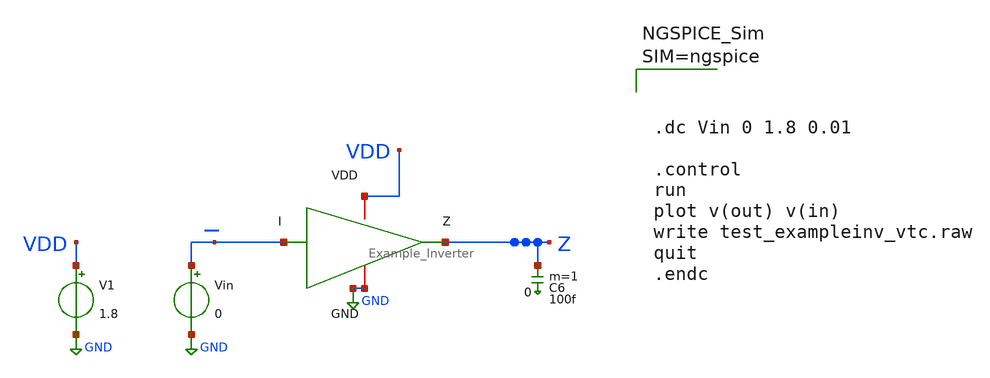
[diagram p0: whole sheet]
** sch_path: sky130_cells/Practice/Example_Inverter/Sims/Example_Inverter_TB_VTC.sch
**.subckt Example_Inverter_TB_VTC
V1 VDD GND 1.8
Vin I GND 0
C6 Z 0 100f m=1
x1 VDD I Z GND Example_Inverter
**** begin user architecture code
 .lib /usr/local/share/pdk/sky130A/libs.tech/ngspice/sky130.lib.spice tt




.dc Vin 0 1.8 0.01

.control
run
plot v(out) v(in)
write test_exampleinv_vtc.raw
quit
.endc



**** end user architecture code
**.ends

* expanding   symbol:  sky130_cells/Practice/Example_Inverter/Example_Inverter.sym # of pins=4
** sym_path: sky130_cells/Practice/Example_Inverter/Example_Inverter.sym
** sch_path: sky130_cells/Practice/Example_Inverter/Example_Inverter.sch
.subckt Example_Inverter VDD I Z GND
*.ipin I
*.opin Z
*.iopin VDD
*.iopin GND
XM1 Z I GND GND sky130_fd_pr__nfet_01v8 L=0.15 W=1 nf=1 ad='int((nf+1)/2) * W/nf * 0.29' as='int((nf+2)/2) * W/nf * 0.29'
+ pd='2*int((nf+1)/2) * (W/nf + 0.29)' ps='2*int((nf+2)/2) * (W/nf + 0.29)' nrd='0.29 / W' nrs='0.29 / W'
+ sa=0 sb=0 sd=0 mult=1 m=1
XM2 Z I VDD VDD sky130_fd_pr__pfet_01v8 L=0.15 W=1 nf=1 ad='int((nf+1)/2) * W/nf * 0.29' as='int((nf+2)/2) * W/nf * 0.29'
+ pd='2*int((nf+1)/2) * (W/nf + 0.29)' ps='2*int((nf+2)/2) * (W/nf + 0.29)' nrd='0.29 / W' nrs='0.29 / W'
+ sa=0 sb=0 sd=0 mult=1 m=1
.ends

.GLOBAL GND
.end
